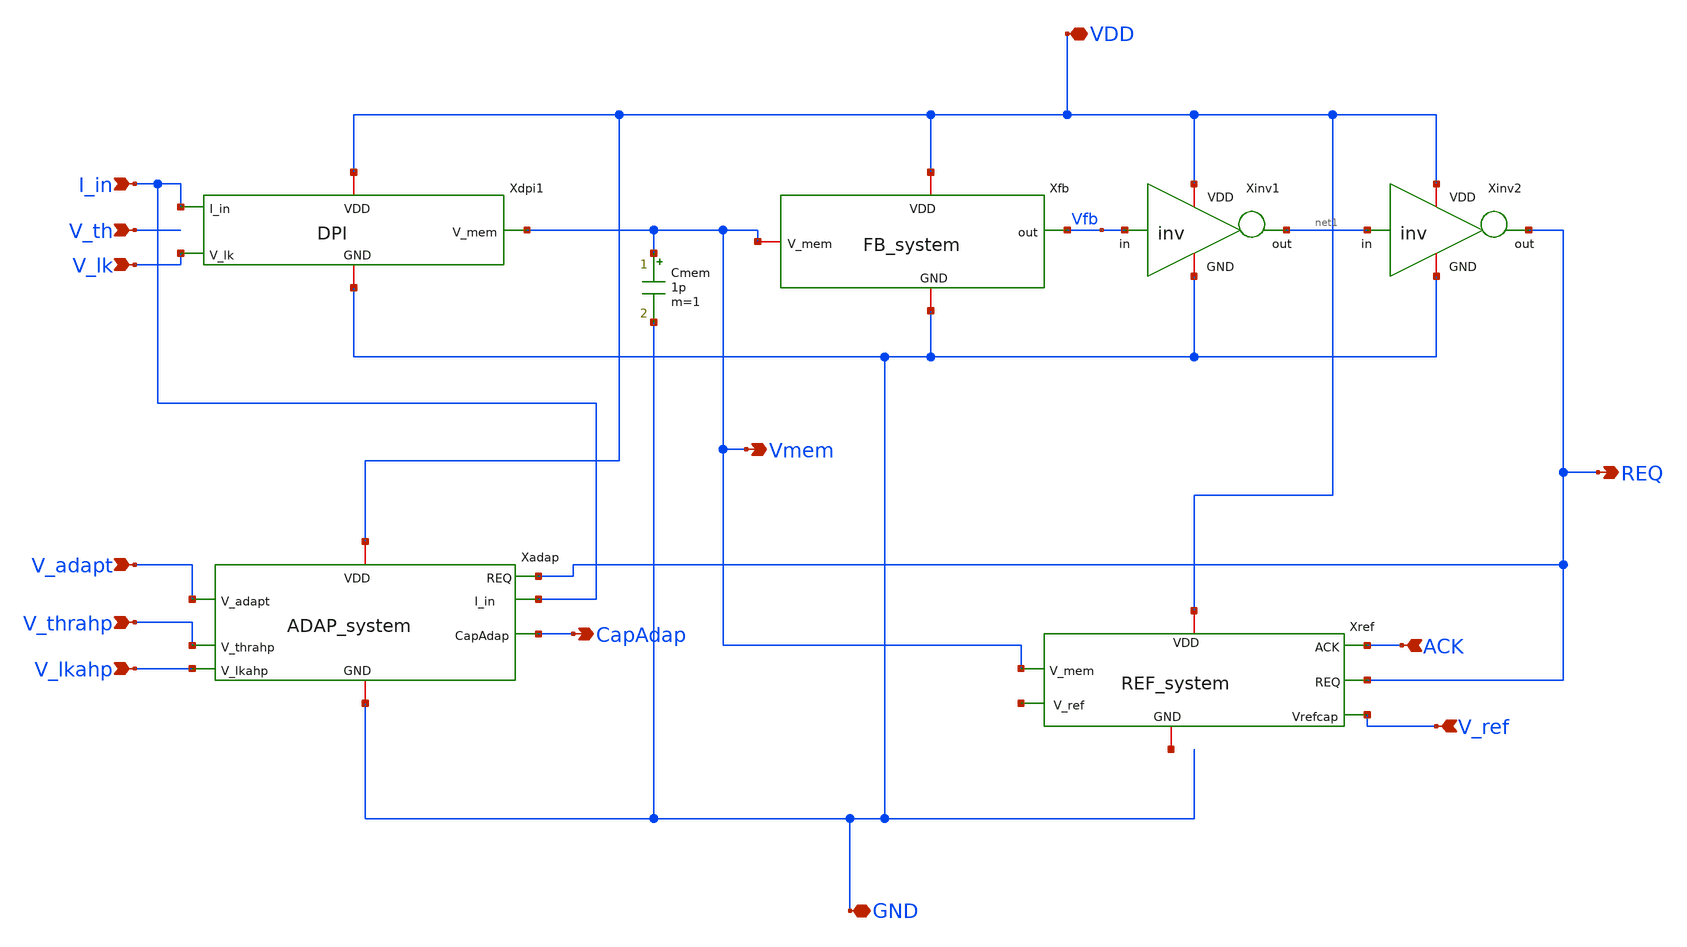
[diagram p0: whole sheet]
** sch_path: xschem/ncs-dpi-adexp/xschem-ncs/neuron.sch
**.subckt neuron V_ref GND VDD REQ ACK I_in V_th V_lk V_adapt V_thrahp V_lkahp CapAdap Vmem
*.ipin V_ref
*.iopin GND
*.iopin VDD
*.opin REQ
*.ipin ACK
*.ipin I_in
*.ipin V_th
*.ipin V_lk
*.ipin V_adapt
*.ipin V_thrahp
*.ipin V_lkahp
*.opin CapAdap
*.opin Vmem
Xinv1 VDD Vfb net1 GND inv
Xinv2 VDD net1 REQ GND inv
Xdpi1 I_in VDD Vmem V_lk GND DPI
Xfb VDD Vfb Vmem GND FB_system
Xadap VDD REQ CapAdap V_adapt I_in V_thrahp V_lkahp GND ADAP_system
Xref ACK Vmem REQ V_ref net2 net3 VDD REF_system
Cmem Vmem GND 1p m=1
**.ends
.end
